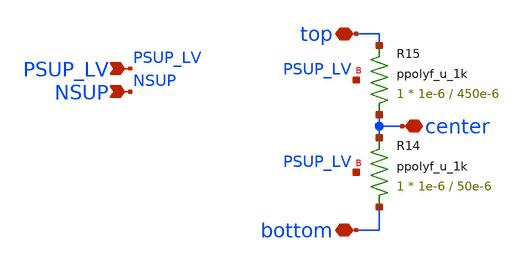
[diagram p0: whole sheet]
** sch_path: xschem/blocks/LPF_gain_fb/LPF_gain_fb.sch
**.subckt LPF_gain_fb top center bottom PSUP_LV NSUP
*.iopin top
*.iopin center
*.iopin bottom
*.ipin PSUP_LV
*.ipin NSUP
XR14 bottom center PSUP_LV ppolyf_u_1k r_width=1e-6 r_length=50e-6 m=1
XR15 center top PSUP_LV ppolyf_u_1k r_width=1e-6 r_length=450e-6 m=1
**.ends
.end
